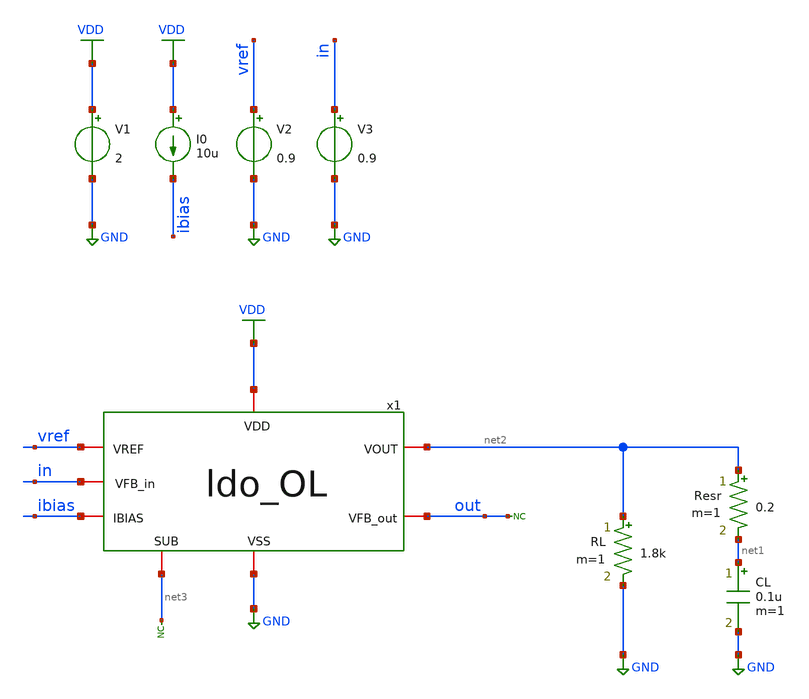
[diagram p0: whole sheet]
** sch_path: designs/libs/tb_ldo/tb_ldo/tb_ldo/tb_ldo_ac/tb_ldo_ac.sch
**.subckt tb_ldo_ac
* noconn #net3
RL net2 GND 1.8k m=1
V1 VDD GND 2
V2 vref GND 0.9
I0 VDD ibias 10u
CL net1 GND 0.1u m=1
Resr net2 net1 0.2 m=1
x1 VDD vref net2 ibias in out net3 GND ldo_OL
V3 in GND 0.9
* noconn out
**** begin user architecture code



.control
save all

** Set sources
alter @V3[AC] = 1

** Simulations
ac dec 100 1 10G

** Plots
setplot ac1
let gain_db = db(v(out))
let phase_deg = cph(-1*v(out))*180/pi
let gain_db_ota = db(v(x1.vota))
let phase_deg_ota = cph(v(x1.vota))*180/pi
plot gain_db
plot phase_deg
plot gain_db_ota
plot phase_deg_ota

** Measurements
meas ac DC_gain FIND gain_db AT=1Hz
let gain_3db = DC_gain-3
meas ac f_3db WHEN gain_db = $&gain_3db
meas ac f_0db WHEN gain_db = 0
meas ac phase_0db FIND phase_deg WHEN gain_db = 0
let phase_margin = 180 + phase_0db
print phase_margin

write tb_ldo_ac.raw
.endc
* ngspice commands




.include $::180MCU_MODELS/design.ngspice
.lib $::180MCU_MODELS/sm141064.ngspice typical
.lib $::180MCU_MODELS/sm141064.ngspice cap_mim
.lib $::180MCU_MODELS/sm141064.ngspice moscap_typical
.lib $::180MCU_MODELS/sm141064.ngspice mimcap_typical
.lib $::180MCU_MODELS/sm141064.ngspice res_typical
* .lib $::180MCU_MODELS/sm141064.ngspice res_statistical
* ngspice commands

**** end user architecture code
**.ends

* expanding   symbol:  libs/core_ldo/ldo/ldo_ldo_OL/ldo_OL.sym # of pins=8
** sym_path: designs/libs/core_ldo/ldo/ldo_ldo_OL/ldo_OL.sym
** sch_path: designs/libs/core_ldo/ldo/ldo_ldo_OL/ldo_OL.sch
.subckt ldo_OL VDD VREF VOUT IBIAS VFB_in VFB_out SUB VSS
*.iopin VFB_out
*.iopin VDD
*.iopin VSS
*.iopin VOUT
*.iopin SUB
*.iopin VREF
*.iopin IBIAS
*.iopin VFB_in
XMp VOUT Vota VDD VDD pfet_05v0 L=0.50u W=100.00u nf=1 ad='int((nf+1)/2) * W/nf * 0.18u' as='int((nf+2)/2) * W/nf * 0.18u'
+ pd='2*int((nf+1)/2) * (W/nf + 0.18u)' ps='2*int((nf+2)/2) * (W/nf + 0.18u)' nrd='0.18u / W' nrs='0.18u / W'
+ sa=0 sb=0 sd=0 m=5
* noconn SUB
x1 VDD VREF VFB_in Vota IBIAS VSS OTA
XR1[3] Vr_fb1[3] VOUT VDD ppolyf_u_1k r_width=1e-6 r_length=5e-6 m=1
XR1[2] Vr_fb1[2] Vr_fb1[3] VDD ppolyf_u_1k r_width=1e-6 r_length=5e-6 m=1
XR1[1] Vr_fb1[1] Vr_fb1[2] VDD ppolyf_u_1k r_width=1e-6 r_length=5e-6 m=1
XR1[0] VFB_out Vr_fb1[1] VDD ppolyf_u_1k r_width=1e-6 r_length=5e-6 m=1
XR2[19] Vr_fb2[19] VFB_out VDD ppolyf_u_1k r_width=1e-6 r_length=5e-6 m=1
XR2[18] Vr_fb2[18] Vr_fb2[19] VDD ppolyf_u_1k r_width=1e-6 r_length=5e-6 m=1
XR2[17] Vr_fb2[17] Vr_fb2[18] VDD ppolyf_u_1k r_width=1e-6 r_length=5e-6 m=1
XR2[16] Vr_fb2[16] Vr_fb2[17] VDD ppolyf_u_1k r_width=1e-6 r_length=5e-6 m=1
XR2[15] Vr_fb2[15] Vr_fb2[16] VDD ppolyf_u_1k r_width=1e-6 r_length=5e-6 m=1
XR2[14] Vr_fb2[14] Vr_fb2[15] VDD ppolyf_u_1k r_width=1e-6 r_length=5e-6 m=1
XR2[13] Vr_fb2[13] Vr_fb2[14] VDD ppolyf_u_1k r_width=1e-6 r_length=5e-6 m=1
XR2[12] Vr_fb2[12] Vr_fb2[13] VDD ppolyf_u_1k r_width=1e-6 r_length=5e-6 m=1
XR2[11] Vr_fb2[11] Vr_fb2[12] VDD ppolyf_u_1k r_width=1e-6 r_length=5e-6 m=1
XR2[10] Vr_fb2[10] Vr_fb2[11] VDD ppolyf_u_1k r_width=1e-6 r_length=5e-6 m=1
XR2[9] Vr_fb2[9] Vr_fb2[10] VDD ppolyf_u_1k r_width=1e-6 r_length=5e-6 m=1
XR2[8] Vr_fb2[8] Vr_fb2[9] VDD ppolyf_u_1k r_width=1e-6 r_length=5e-6 m=1
XR2[7] Vr_fb2[7] Vr_fb2[8] VDD ppolyf_u_1k r_width=1e-6 r_length=5e-6 m=1
XR2[6] Vr_fb2[6] Vr_fb2[7] VDD ppolyf_u_1k r_width=1e-6 r_length=5e-6 m=1
XR2[5] Vr_fb2[5] Vr_fb2[6] VDD ppolyf_u_1k r_width=1e-6 r_length=5e-6 m=1
XR2[4] Vr_fb2[4] Vr_fb2[5] VDD ppolyf_u_1k r_width=1e-6 r_length=5e-6 m=1
XR2[3] Vr_fb2[3] Vr_fb2[4] VDD ppolyf_u_1k r_width=1e-6 r_length=5e-6 m=1
XR2[2] Vr_fb2[2] Vr_fb2[3] VDD ppolyf_u_1k r_width=1e-6 r_length=5e-6 m=1
XR2[1] Vr_fb2[1] Vr_fb2[2] VDD ppolyf_u_1k r_width=1e-6 r_length=5e-6 m=1
XR2[0] VSS Vr_fb2[1] VDD ppolyf_u_1k r_width=1e-6 r_length=5e-6 m=1
XRc[29] Vr_mc[29] Vmc VDD ppolyf_u_1k r_width=1e-6 r_length=10e-6 m=1
XRc[28] Vr_mc[28] Vr_mc[29] VDD ppolyf_u_1k r_width=1e-6 r_length=10e-6 m=1
XRc[27] Vr_mc[27] Vr_mc[28] VDD ppolyf_u_1k r_width=1e-6 r_length=10e-6 m=1
XRc[26] Vr_mc[26] Vr_mc[27] VDD ppolyf_u_1k r_width=1e-6 r_length=10e-6 m=1
XRc[25] Vr_mc[25] Vr_mc[26] VDD ppolyf_u_1k r_width=1e-6 r_length=10e-6 m=1
XRc[24] Vr_mc[24] Vr_mc[25] VDD ppolyf_u_1k r_width=1e-6 r_length=10e-6 m=1
XRc[23] Vr_mc[23] Vr_mc[24] VDD ppolyf_u_1k r_width=1e-6 r_length=10e-6 m=1
XRc[22] Vr_mc[22] Vr_mc[23] VDD ppolyf_u_1k r_width=1e-6 r_length=10e-6 m=1
XRc[21] Vr_mc[21] Vr_mc[22] VDD ppolyf_u_1k r_width=1e-6 r_length=10e-6 m=1
XRc[20] Vr_mc[20] Vr_mc[21] VDD ppolyf_u_1k r_width=1e-6 r_length=10e-6 m=1
XRc[19] Vr_mc[19] Vr_mc[20] VDD ppolyf_u_1k r_width=1e-6 r_length=10e-6 m=1
XRc[18] Vr_mc[18] Vr_mc[19] VDD ppolyf_u_1k r_width=1e-6 r_length=10e-6 m=1
XRc[17] Vr_mc[17] Vr_mc[18] VDD ppolyf_u_1k r_width=1e-6 r_length=10e-6 m=1
XRc[16] Vr_mc[16] Vr_mc[17] VDD ppolyf_u_1k r_width=1e-6 r_length=10e-6 m=1
XRc[15] Vr_mc[15] Vr_mc[16] VDD ppolyf_u_1k r_width=1e-6 r_length=10e-6 m=1
XRc[14] Vr_mc[14] Vr_mc[15] VDD ppolyf_u_1k r_width=1e-6 r_length=10e-6 m=1
XRc[13] Vr_mc[13] Vr_mc[14] VDD ppolyf_u_1k r_width=1e-6 r_length=10e-6 m=1
XRc[12] Vr_mc[12] Vr_mc[13] VDD ppolyf_u_1k r_width=1e-6 r_length=10e-6 m=1
XRc[11] Vr_mc[11] Vr_mc[12] VDD ppolyf_u_1k r_width=1e-6 r_length=10e-6 m=1
XRc[10] Vr_mc[10] Vr_mc[11] VDD ppolyf_u_1k r_width=1e-6 r_length=10e-6 m=1
XRc[9] Vr_mc[9] Vr_mc[10] VDD ppolyf_u_1k r_width=1e-6 r_length=10e-6 m=1
XRc[8] Vr_mc[8] Vr_mc[9] VDD ppolyf_u_1k r_width=1e-6 r_length=10e-6 m=1
XRc[7] Vr_mc[7] Vr_mc[8] VDD ppolyf_u_1k r_width=1e-6 r_length=10e-6 m=1
XRc[6] Vr_mc[6] Vr_mc[7] VDD ppolyf_u_1k r_width=1e-6 r_length=10e-6 m=1
XRc[5] Vr_mc[5] Vr_mc[6] VDD ppolyf_u_1k r_width=1e-6 r_length=10e-6 m=1
XRc[4] Vr_mc[4] Vr_mc[5] VDD ppolyf_u_1k r_width=1e-6 r_length=10e-6 m=1
XRc[3] Vr_mc[3] Vr_mc[4] VDD ppolyf_u_1k r_width=1e-6 r_length=10e-6 m=1
XRc[2] Vr_mc[2] Vr_mc[3] VDD ppolyf_u_1k r_width=1e-6 r_length=10e-6 m=1
XRc[1] Vr_mc[1] Vr_mc[2] VDD ppolyf_u_1k r_width=1e-6 r_length=10e-6 m=1
XRc[0] VOUT Vr_mc[1] VDD ppolyf_u_1k r_width=1e-6 r_length=10e-6 m=1
XCc Vota Vmc cap_mim_1f0fF c_width=25e-6 c_length=25e-6 m=4
XRfb_dummy_L[7] VSS VSS VSS ppolyf_u_1k r_width=1e-6 r_length=5e-6 m=1
XRfb_dummy_L[6] VSS VSS VSS ppolyf_u_1k r_width=1e-6 r_length=5e-6 m=1
XRfb_dummy_L[5] VSS VSS VSS ppolyf_u_1k r_width=1e-6 r_length=5e-6 m=1
XRfb_dummy_L[4] VSS VSS VSS ppolyf_u_1k r_width=1e-6 r_length=5e-6 m=1
XRfb_dummy_L[3] VSS VSS VSS ppolyf_u_1k r_width=1e-6 r_length=5e-6 m=1
XRfb_dummy_L[2] VSS VSS VSS ppolyf_u_1k r_width=1e-6 r_length=5e-6 m=1
XRfb_dummy_L[1] VSS VSS VSS ppolyf_u_1k r_width=1e-6 r_length=5e-6 m=1
XRfb_dummy_L[0] VSS VSS VSS ppolyf_u_1k r_width=1e-6 r_length=5e-6 m=1
XRfb_dummy_TB[15] VSS VSS VSS ppolyf_u_1k r_width=1e-6 r_length=5e-6 m=1
XRfb_dummy_TB[14] VSS VSS VSS ppolyf_u_1k r_width=1e-6 r_length=5e-6 m=1
XRfb_dummy_TB[13] VSS VSS VSS ppolyf_u_1k r_width=1e-6 r_length=5e-6 m=1
XRfb_dummy_TB[12] VSS VSS VSS ppolyf_u_1k r_width=1e-6 r_length=5e-6 m=1
XRfb_dummy_TB[11] VSS VSS VSS ppolyf_u_1k r_width=1e-6 r_length=5e-6 m=1
XRfb_dummy_TB[10] VSS VSS VSS ppolyf_u_1k r_width=1e-6 r_length=5e-6 m=1
XRfb_dummy_TB[9] VSS VSS VSS ppolyf_u_1k r_width=1e-6 r_length=5e-6 m=1
XRfb_dummy_TB[8] VSS VSS VSS ppolyf_u_1k r_width=1e-6 r_length=5e-6 m=1
XRfb_dummy_TB[7] VSS VSS VSS ppolyf_u_1k r_width=1e-6 r_length=5e-6 m=1
XRfb_dummy_TB[6] VSS VSS VSS ppolyf_u_1k r_width=1e-6 r_length=5e-6 m=1
XRfb_dummy_TB[5] VSS VSS VSS ppolyf_u_1k r_width=1e-6 r_length=5e-6 m=1
XRfb_dummy_TB[4] VSS VSS VSS ppolyf_u_1k r_width=1e-6 r_length=5e-6 m=1
XRfb_dummy_TB[3] VSS VSS VSS ppolyf_u_1k r_width=1e-6 r_length=5e-6 m=1
XRfb_dummy_TB[2] VSS VSS VSS ppolyf_u_1k r_width=1e-6 r_length=5e-6 m=1
XRfb_dummy_TB[1] VSS VSS VSS ppolyf_u_1k r_width=1e-6 r_length=5e-6 m=1
XRfb_dummy_TB[0] VSS VSS VSS ppolyf_u_1k r_width=1e-6 r_length=5e-6 m=1
.ends


* expanding   symbol:  libs/core_ldo/ldo/ldo_OTA/OTA.sym # of pins=6
** sym_path: designs/libs/core_ldo/ldo/OTA.sym
** sch_path: designs/libs/core_ldo/ldo/OTA.sch
.subckt OTA VDD VREF VFB VOTA IBIAS VSS
*.iopin VDD
*.iopin VSS
*.iopin VOTA
*.iopin VREF
*.iopin IBIAS
*.iopin VFB
XM3 net2 net2 VDD VDD pfet_05v0 L=2.00u W=8.00u nf=1 ad='int((nf+1)/2) * W/nf * 0.18u' as='int((nf+2)/2) * W/nf * 0.18u'
+ pd='2*int((nf+1)/2) * (W/nf + 0.18u)' ps='2*int((nf+2)/2) * (W/nf + 0.18u)' nrd='0.18u / W' nrs='0.18u / W'
+ sa=0 sb=0 sd=0 m=1
XM4 net3 net3 VDD VDD pfet_05v0 L=2.00u W=8.00u nf=1 ad='int((nf+1)/2) * W/nf * 0.18u' as='int((nf+2)/2) * W/nf * 0.18u'
+ pd='2*int((nf+1)/2) * (W/nf + 0.18u)' ps='2*int((nf+2)/2) * (W/nf + 0.18u)' nrd='0.18u / W' nrs='0.18u / W'
+ sa=0 sb=0 sd=0 m=1
XM5 net4 net2 VDD VDD pfet_05v0 L=2.00u W=8.00u nf=1 ad='int((nf+1)/2) * W/nf * 0.18u' as='int((nf+2)/2) * W/nf * 0.18u'
+ pd='2*int((nf+1)/2) * (W/nf + 0.18u)' ps='2*int((nf+2)/2) * (W/nf + 0.18u)' nrd='0.18u / W' nrs='0.18u / W'
+ sa=0 sb=0 sd=0 m=1
XM6 VOTA net3 VDD VDD pfet_05v0 L=2.00u W=8.00u nf=1 ad='int((nf+1)/2) * W/nf * 0.18u' as='int((nf+2)/2) * W/nf * 0.18u'
+ pd='2*int((nf+1)/2) * (W/nf + 0.18u)' ps='2*int((nf+2)/2) * (W/nf + 0.18u)' nrd='0.18u / W' nrs='0.18u / W'
+ sa=0 sb=0 sd=0 m=2
XM9 IBIAS IBIAS VSS VSS nfet_05v0 L=2.00u W=4.00u nf=1 ad='int((nf+1)/2) * W/nf * 0.18u' as='int((nf+2)/2) * W/nf * 0.18u'
+ pd='2*int((nf+1)/2) * (W/nf + 0.18u)' ps='2*int((nf+2)/2) * (W/nf + 0.18u)' nrd='0.18u / W' nrs='0.18u / W'
+ sa=0 sb=0 sd=0 m=1
XM10 net1 IBIAS VSS VSS nfet_05v0 L=2.00u W=4.00u nf=1 ad='int((nf+1)/2) * W/nf * 0.18u' as='int((nf+2)/2) * W/nf * 0.18u'
+ pd='2*int((nf+1)/2) * (W/nf + 0.18u)' ps='2*int((nf+2)/2) * (W/nf + 0.18u)' nrd='0.18u / W' nrs='0.18u / W'
+ sa=0 sb=0 sd=0 m=1
XM7 net4 net4 VSS VSS nfet_05v0 L=2.00u W=4.00u nf=1 ad='int((nf+1)/2) * W/nf * 0.18u' as='int((nf+2)/2) * W/nf * 0.18u'
+ pd='2*int((nf+1)/2) * (W/nf + 0.18u)' ps='2*int((nf+2)/2) * (W/nf + 0.18u)' nrd='0.18u / W' nrs='0.18u / W'
+ sa=0 sb=0 sd=0 m=1
XM8 VOTA net4 VSS VSS nfet_05v0 L=2.00u W=4.00u nf=1 ad='int((nf+1)/2) * W/nf * 0.18u' as='int((nf+2)/2) * W/nf * 0.18u'
+ pd='2*int((nf+1)/2) * (W/nf + 0.18u)' ps='2*int((nf+2)/2) * (W/nf + 0.18u)' nrd='0.18u / W' nrs='0.18u / W'
+ sa=0 sb=0 sd=0 m=2
XM1 net2 VREF net1 net1 nfet_05v0 L=0.60u W=40.00u nf=1 ad='int((nf+1)/2) * W/nf * 0.18u' as='int((nf+2)/2) * W/nf * 0.18u'
+ pd='2*int((nf+1)/2) * (W/nf + 0.18u)' ps='2*int((nf+2)/2) * (W/nf + 0.18u)' nrd='0.18u / W' nrs='0.18u / W'
+ sa=0 sb=0 sd=0 m=1
XM2 net3 VFB net1 net1 nfet_05v0 L=0.60u W=40.00u nf=1 ad='int((nf+1)/2) * W/nf * 0.18u' as='int((nf+2)/2) * W/nf * 0.18u'
+ pd='2*int((nf+1)/2) * (W/nf + 0.18u)' ps='2*int((nf+2)/2) * (W/nf + 0.18u)' nrd='0.18u / W' nrs='0.18u / W'
+ sa=0 sb=0 sd=0 m=1
.ends

.GLOBAL GND
.GLOBAL VDD
.end
